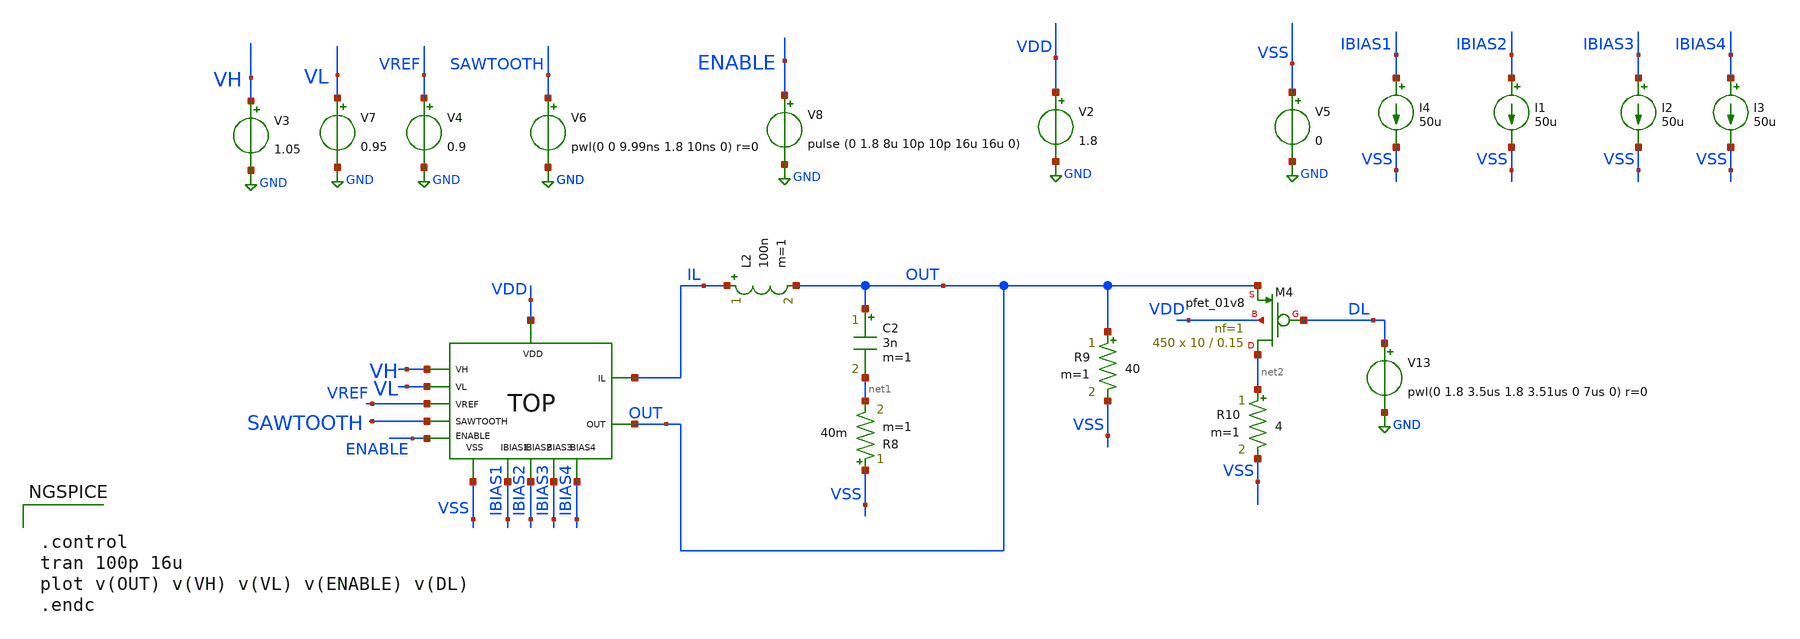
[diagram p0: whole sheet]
** sch_path: xschem/DC_DC_Converter_xschem/DC_DC_Converter/TOP_LEVEL/Top_Final/Top_TB.sch
**.subckt Top_TB
V2 VDD GND 1.8
V5 VSS GND 0
V4 VREF GND 0.9
V6 SAWTOOTH GND pwl(0 0 9.99ns 1.8 10ns 0) r=0
V3 VH GND 1.05
V7 VL GND 0.95
V8 ENABLE GND pulse (0 1.8 8u 10p 10p 16u 16u 0)
L2 IL OUT 100n m=1
C2 OUT net1 3n m=1
R8 VSS net1 40m m=1
XM4 net2 DL OUT VDD sky130_fd_pr__pfet_01v8 L=0.15 W=10 nf=1 ad='int((nf+1)/2) * W/nf * 0.29' as='int((nf+2)/2) * W/nf * 0.29'
+ pd='2*int((nf+1)/2) * (W/nf + 0.29)' ps='2*int((nf+2)/2) * (W/nf + 0.29)' nrd='0.29 / W' nrs='0.29 / W'
+ sa=0 sb=0 sd=0 mult=450 m=450
V13 DL GND pwl(0 1.8 3.5us 1.8 3.51us 0 7us 0) r=0
R9 OUT VSS 40 m=1
R10 net2 VSS 4 m=1
x1 VDD VSS VREF IL VH IBIAS1 VL IBIAS2 ENABLE IBIAS3 OUT IBIAS4 SAWTOOTH Top
I4 IBIAS1 VSS 50u
I1 IBIAS2 VSS 50u
I2 IBIAS3 VSS 50u
I3 IBIAS4 VSS 50u
**** begin user architecture code


.control
tran 100p 16u
plot v(OUT) v(VH) v(VL) v(ENABLE) v(DL)
.endc


** manual skywater pdks install (with patches applied)
* .lib $::SKYWATER_MODELS/models/sky130.lib.spice tt

** opencircuitdesign pdks install
.lib $::SKYWATER_MODELS/sky130.lib.spice tt
.include $::SKYWATER_STDCELLS/sky130_fd_sc_hd.spice

**** end user architecture code
**.ends
.GLOBAL GND
.end
